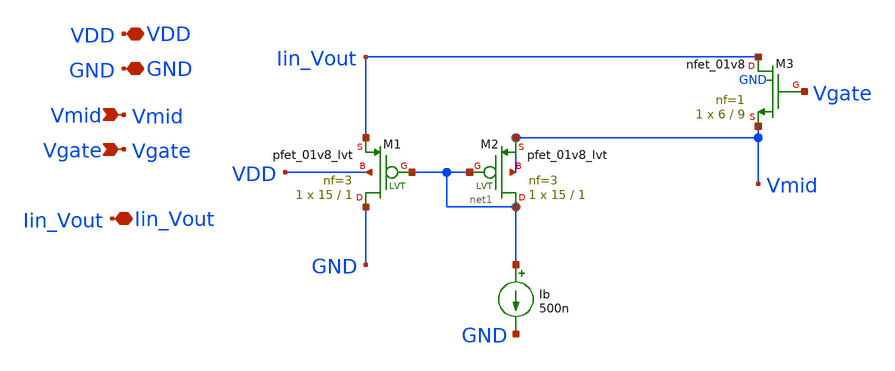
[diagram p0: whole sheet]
** sch_path: sch/summing_stage/iv_clamp.sch
**.subckt iv_clamp Vmid VDD GND Vgate Iin_Vout
*.ipin Vmid
*.iopin VDD
*.iopin GND
*.ipin Vgate
*.iopin Iin_Vout
XM3 Iin_Vout Vgate Vmid GND sky130_fd_pr__nfet_01v8 L=9 W=6 nf=1 ad='int((1 + 1)/2) * 6 / 1 * 0.29' as='int((1 + 2)/2) * 6 / 1 * 0.29'
+ pd='2*int((1 + 1)/2) * (6 / 1 + 0.29)' ps='2*int((1 + 2)/2) * (6 / 1 + 0.29)' nrd='0.29 / 6 ' nrs='0.29 / 6 '
+ sa=0 sb=0 sd=0 mult=1 m=1
XM1 GND net1 Iin_Vout VDD sky130_fd_pr__pfet_01v8_lvt L=1 W=15 nf=3 ad='int((3 + 1)/2) * 15 / 3 * 0.29'
+ as='int((3 + 2)/2) * 15 / 3 * 0.29' pd='2*int((3 + 1)/2) * (15 / 3 + 0.29)' ps='2*int((3 + 2)/2) * (15 / 3 + 0.29)'
+ nrd='0.29 / 15 ' nrs='0.29 / 15 ' sa=0 sb=0 sd=0 mult=1 m=1
XM2 net1 net1 Vmid Vmid sky130_fd_pr__pfet_01v8_lvt L=1 W=15 nf=3 ad='int((3 + 1)/2) * 15 / 3 * 0.29'
+ as='int((3 + 2)/2) * 15 / 3 * 0.29' pd='2*int((3 + 1)/2) * (15 / 3 + 0.29)' ps='2*int((3 + 2)/2) * (15 / 3 + 0.29)'
+ nrd='0.29 / 15 ' nrs='0.29 / 15 ' sa=0 sb=0 sd=0 mult=1 m=1
Ib net1 GND 500n
**.ends
.end
